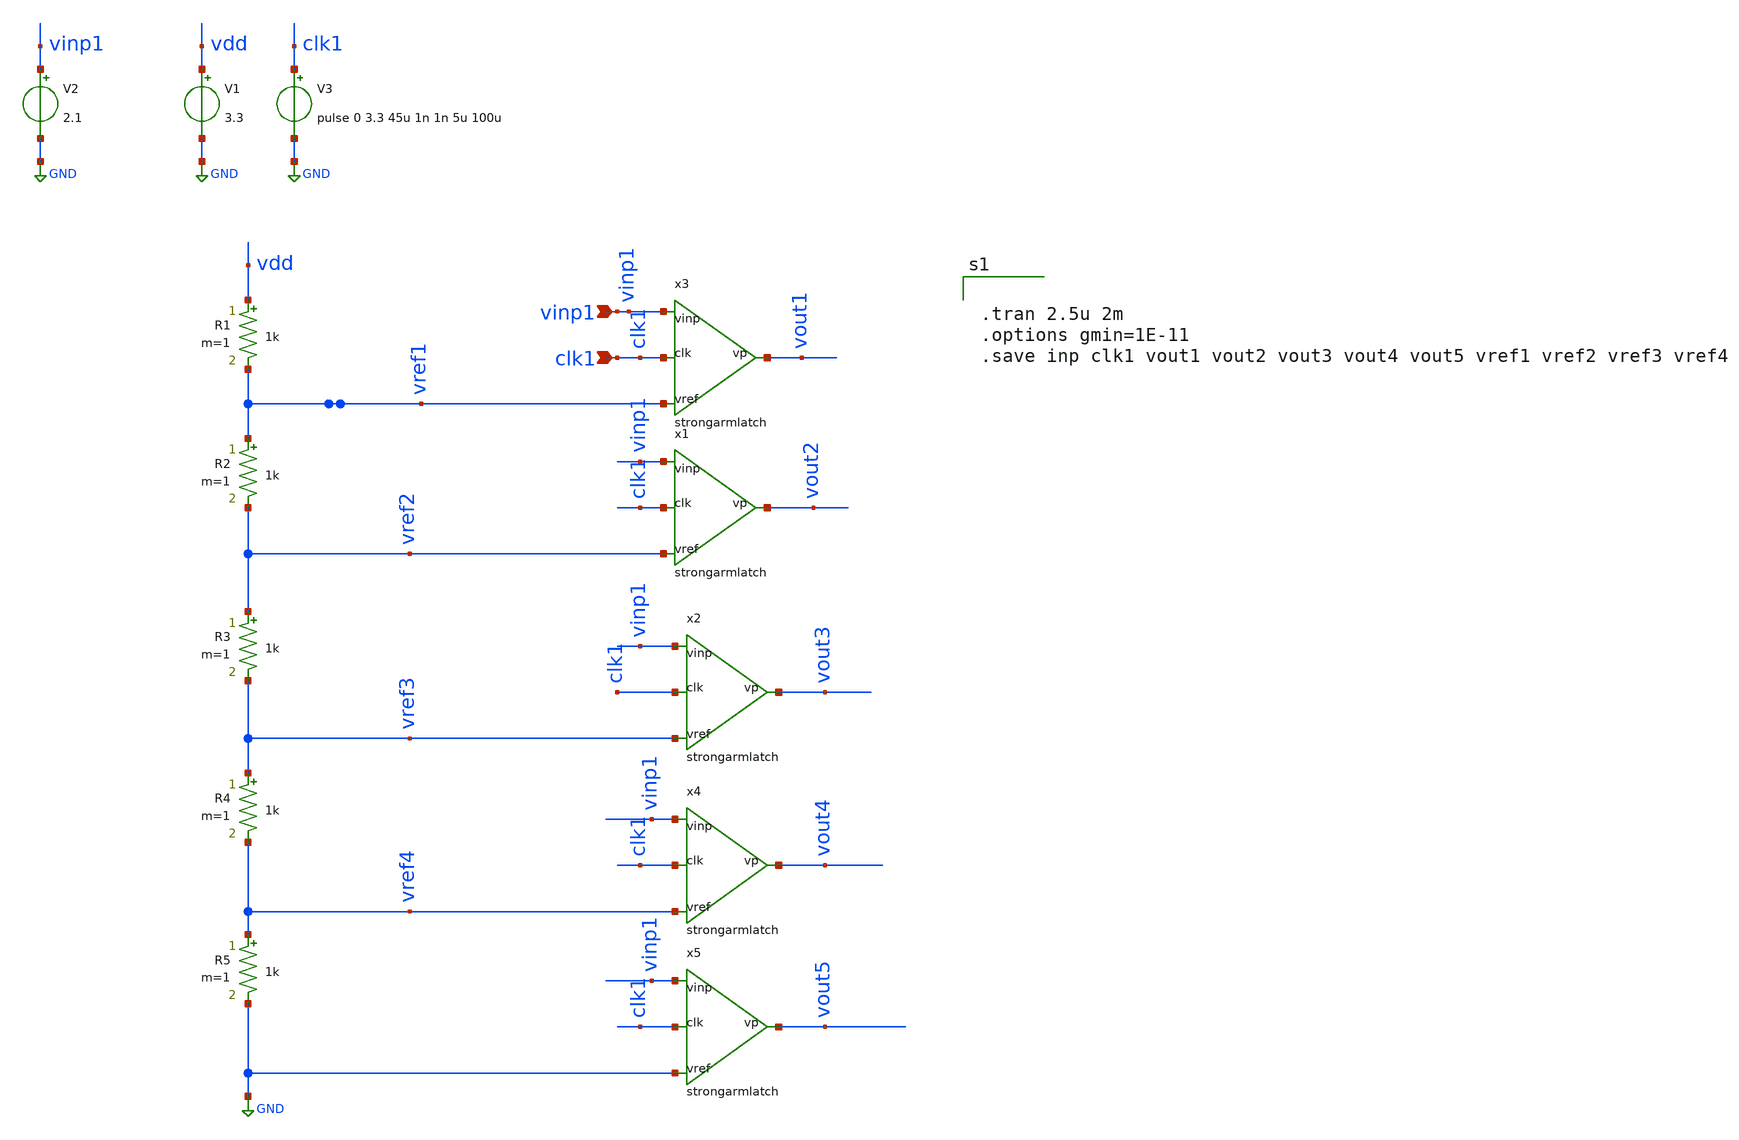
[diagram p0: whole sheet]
** sch_path: xschem/FDC/strongarmlatchtest.sch
**.subckt strongarmlatchtest vinp1 clk1
*.ipin vinp1
*.ipin clk1
V1 vdd GND 3.3
x3 vinp1 vref1 vout1 clk1 strongarmlatch
V2 vinp1 GND 2.1
V3 clk1 GND pulse 0 3.3 45u 1n 1n 5u 100u
R1 vdd vref1 1k m=1
R2 vref1 vref2 1k m=1
R3 vref2 vref3 1k m=1
R4 vref3 vref4 1k m=1
R5 vref4 GND 1k m=1
x1 vinp1 vref2 vout2 clk1 strongarmlatch
x2 vinp1 vref3 vout3 clk1 strongarmlatch
x4 vinp1 vref4 vout4 clk1 strongarmlatch
x5 vinp1 GND vout5 clk1 strongarmlatch
**** begin user architecture code

.lib ~/open_pdks/sky130/sky130A/libs.tech/ngspice/sky130.lib.spice tt
.include /home/vinodhini/open_pdks/sky130/sky130A/libs.ref/sky130_fd_sc_hvl/spice/sky130_fd_sc_hvl.spice

*.MODEL swmod SW(VT=0.0 VH=0.01 RON=1 ROFF=10000000000)
.param mc_mm_switch=0
.param mc_pr_switch=0


.tran 2.5u 2m
.options gmin=1E-11
.save inp clk1 vout1 vout2 vout3 vout4 vout5 vref1 vref2 vref3 vref4

**** end user architecture code
**.ends

* expanding   symbol:  /home/vinodhini/Documents/strongarmlatch.sym # of pins=4
** sym_path: xschem/FDC/strongarmlatch.sym
** sch_path: xschem/FDC/strongarmlatch.sch
.subckt strongarmlatch vinp vref vp clk
*.ipin vinp
*.ipin vref
*.ipin clk
*.opin vp
XM7 net5 vinp net3 GND sky130_fd_pr__nfet_g5v0d10v5 L=0.5 W=12 nf=1 ad='int((nf+1)/2) * W/nf * 0.29'
+ as='int((nf+2)/2) * W/nf * 0.29' pd='2*int((nf+1)/2) * (W/nf + 0.29)' ps='2*int((nf+2)/2) * (W/nf + 0.29)'
+ nrd='0.29 / W' nrs='0.29 / W' sa=0 sb=0 sd=0 mult=1 m=1
XM8 net4 vref net3 GND sky130_fd_pr__nfet_g5v0d10v5 L=0.5 W=12 nf=1 ad='int((nf+1)/2) * W/nf * 0.29'
+ as='int((nf+2)/2) * W/nf * 0.29' pd='2*int((nf+1)/2) * (W/nf + 0.29)' ps='2*int((nf+2)/2) * (W/nf + 0.29)'
+ nrd='0.29 / W' nrs='0.29 / W' sa=0 sb=0 sd=0 mult=1 m=1
XM3 net2 net1 vdda vdda sky130_fd_pr__pfet_g5v0d10v5 L=0.5 W=8 nf=1 ad='int((nf+1)/2) * W/nf * 0.29'
+ as='int((nf+2)/2) * W/nf * 0.29' pd='2*int((nf+1)/2) * (W/nf + 0.29)' ps='2*int((nf+2)/2) * (W/nf + 0.29)'
+ nrd='0.29 / W' nrs='0.29 / W' sa=0 sb=0 sd=0 mult=1 m=1
XM9 net2 clk vdda vdda sky130_fd_pr__pfet_g5v0d10v5 L=0.5 W=8 nf=1 ad='int((nf+1)/2) * W/nf * 0.29' as='int((nf+2)/2) * W/nf * 0.29'
+ pd='2*int((nf+1)/2) * (W/nf + 0.29)' ps='2*int((nf+2)/2) * (W/nf + 0.29)' nrd='0.29 / W' nrs='0.29 / W'
+ sa=0 sb=0 sd=0 mult=1 m=1
XM4 net1 clk vdda vdda sky130_fd_pr__pfet_g5v0d10v5 L=0.5 W=8 nf=1 ad='int((nf+1)/2) * W/nf * 0.29' as='int((nf+2)/2) * W/nf * 0.29'
+ pd='2*int((nf+1)/2) * (W/nf + 0.29)' ps='2*int((nf+2)/2) * (W/nf + 0.29)' nrd='0.29 / W' nrs='0.29 / W'
+ sa=0 sb=0 sd=0 mult=1 m=1
XM10 net1 net2 vdda vdda sky130_fd_pr__pfet_g5v0d10v5 L=0.5 W=8 nf=1 ad='int((nf+1)/2) * W/nf * 0.29'
+ as='int((nf+2)/2) * W/nf * 0.29' pd='2*int((nf+1)/2) * (W/nf + 0.29)' ps='2*int((nf+2)/2) * (W/nf + 0.29)'
+ nrd='0.29 / W' nrs='0.29 / W' sa=0 sb=0 sd=0 mult=1 m=1
XM11 net4 clk vdda vdda sky130_fd_pr__pfet_g5v0d10v5 L=0.5 W=8 nf=1 ad='int((nf+1)/2) * W/nf * 0.29'
+ as='int((nf+2)/2) * W/nf * 0.29' pd='2*int((nf+1)/2) * (W/nf + 0.29)' ps='2*int((nf+2)/2) * (W/nf + 0.29)'
+ nrd='0.29 / W' nrs='0.29 / W' sa=0 sb=0 sd=0 mult=1 m=1
XM12 net5 clk vdda vdda sky130_fd_pr__pfet_g5v0d10v5 L=0.5 W=8 nf=1 ad='int((nf+1)/2) * W/nf * 0.29'
+ as='int((nf+2)/2) * W/nf * 0.29' pd='2*int((nf+1)/2) * (W/nf + 0.29)' ps='2*int((nf+2)/2) * (W/nf + 0.29)'
+ nrd='0.29 / W' nrs='0.29 / W' sa=0 sb=0 sd=0 mult=1 m=1
XM13 net3 clk vssa vssa sky130_fd_pr__nfet_g5v0d10v5 L=0.5 W=8 nf=1 ad='int((nf+1)/2) * W/nf * 0.29'
+ as='int((nf+2)/2) * W/nf * 0.29' pd='2*int((nf+1)/2) * (W/nf + 0.29)' ps='2*int((nf+2)/2) * (W/nf + 0.29)'
+ nrd='0.29 / W' nrs='0.29 / W' sa=0 sb=0 sd=0 mult=1 m=1
XM14 net3 vinp net4 vdda sky130_fd_pr__pfet_g5v0d10v5 L=0.5 W=8 nf=1 ad='int((nf+1)/2) * W/nf * 0.29'
+ as='int((nf+2)/2) * W/nf * 0.29' pd='2*int((nf+1)/2) * (W/nf + 0.29)' ps='2*int((nf+2)/2) * (W/nf + 0.29)'
+ nrd='0.29 / W' nrs='0.29 / W' sa=0 sb=0 sd=0 mult=1 m=1
XM15 net3 vref net5 vdda sky130_fd_pr__pfet_g5v0d10v5 L=0.5 W=8 nf=1 ad='int((nf+1)/2) * W/nf * 0.29'
+ as='int((nf+2)/2) * W/nf * 0.29' pd='2*int((nf+1)/2) * (W/nf + 0.29)' ps='2*int((nf+2)/2) * (W/nf + 0.29)'
+ nrd='0.29 / W' nrs='0.29 / W' sa=0 sb=0 sd=0 mult=1 m=1
XM16 vm vop GND GND sky130_fd_pr__nfet_g5v0d10v5 L=0.5 W=1 nf=1 ad='int((nf+1)/2) * W/nf * 0.29' as='int((nf+2)/2) * W/nf * 0.29'
+ pd='2*int((nf+1)/2) * (W/nf + 0.29)' ps='2*int((nf+2)/2) * (W/nf + 0.29)' nrd='0.29 / W' nrs='0.29 / W'
+ sa=0 sb=0 sd=0 mult=1 m=1
XM17 vp vom GND GND sky130_fd_pr__nfet_g5v0d10v5 L=0.5 W=1 nf=1 ad='int((nf+1)/2) * W/nf * 0.29' as='int((nf+2)/2) * W/nf * 0.29'
+ pd='2*int((nf+1)/2) * (W/nf + 0.29)' ps='2*int((nf+2)/2) * (W/nf + 0.29)' nrd='0.29 / W' nrs='0.29 / W'
+ sa=0 sb=0 sd=0 mult=1 m=1
XM1 net2 net1 net5 GND sky130_fd_pr__nfet_g5v0d10v5 L=0.5 W=4 nf=1 ad='int((nf+1)/2) * W/nf * 0.29' as='int((nf+2)/2) * W/nf * 0.29'
+ pd='2*int((nf+1)/2) * (W/nf + 0.29)' ps='2*int((nf+2)/2) * (W/nf + 0.29)' nrd='0.29 / W' nrs='0.29 / W'
+ sa=0 sb=0 sd=0 mult=1 m=1
XM2 net1 net2 net4 GND sky130_fd_pr__nfet_g5v0d10v5 L=0.5 W=4 nf=1 ad='int((nf+1)/2) * W/nf * 0.29' as='int((nf+2)/2) * W/nf * 0.29'
+ pd='2*int((nf+1)/2) * (W/nf + 0.29)' ps='2*int((nf+2)/2) * (W/nf + 0.29)' nrd='0.29 / W' nrs='0.29 / W'
+ sa=0 sb=0 sd=0 mult=1 m=1
x1 net1 VGND VNB VPB VPWR vom sky130_fd_sc_hvl__inv_1
x2 net2 VGND VNB VPB VPWR vop sky130_fd_sc_hvl__inv_1
x4 vm VGND VNB VPB VPWR vp sky130_fd_sc_hvl__inv_1
x3 vp VGND VNB VPB VPWR vm sky130_fd_sc_hvl__inv_1
V1 vdda vssa 3.3
V2 vssa GND 0
V3 VPWR vssa 3.3
V4 VPB vssa 3.3
V5 VGND vssa 0
V6 VNB vssa 0
.ends

.GLOBAL GND
.end
